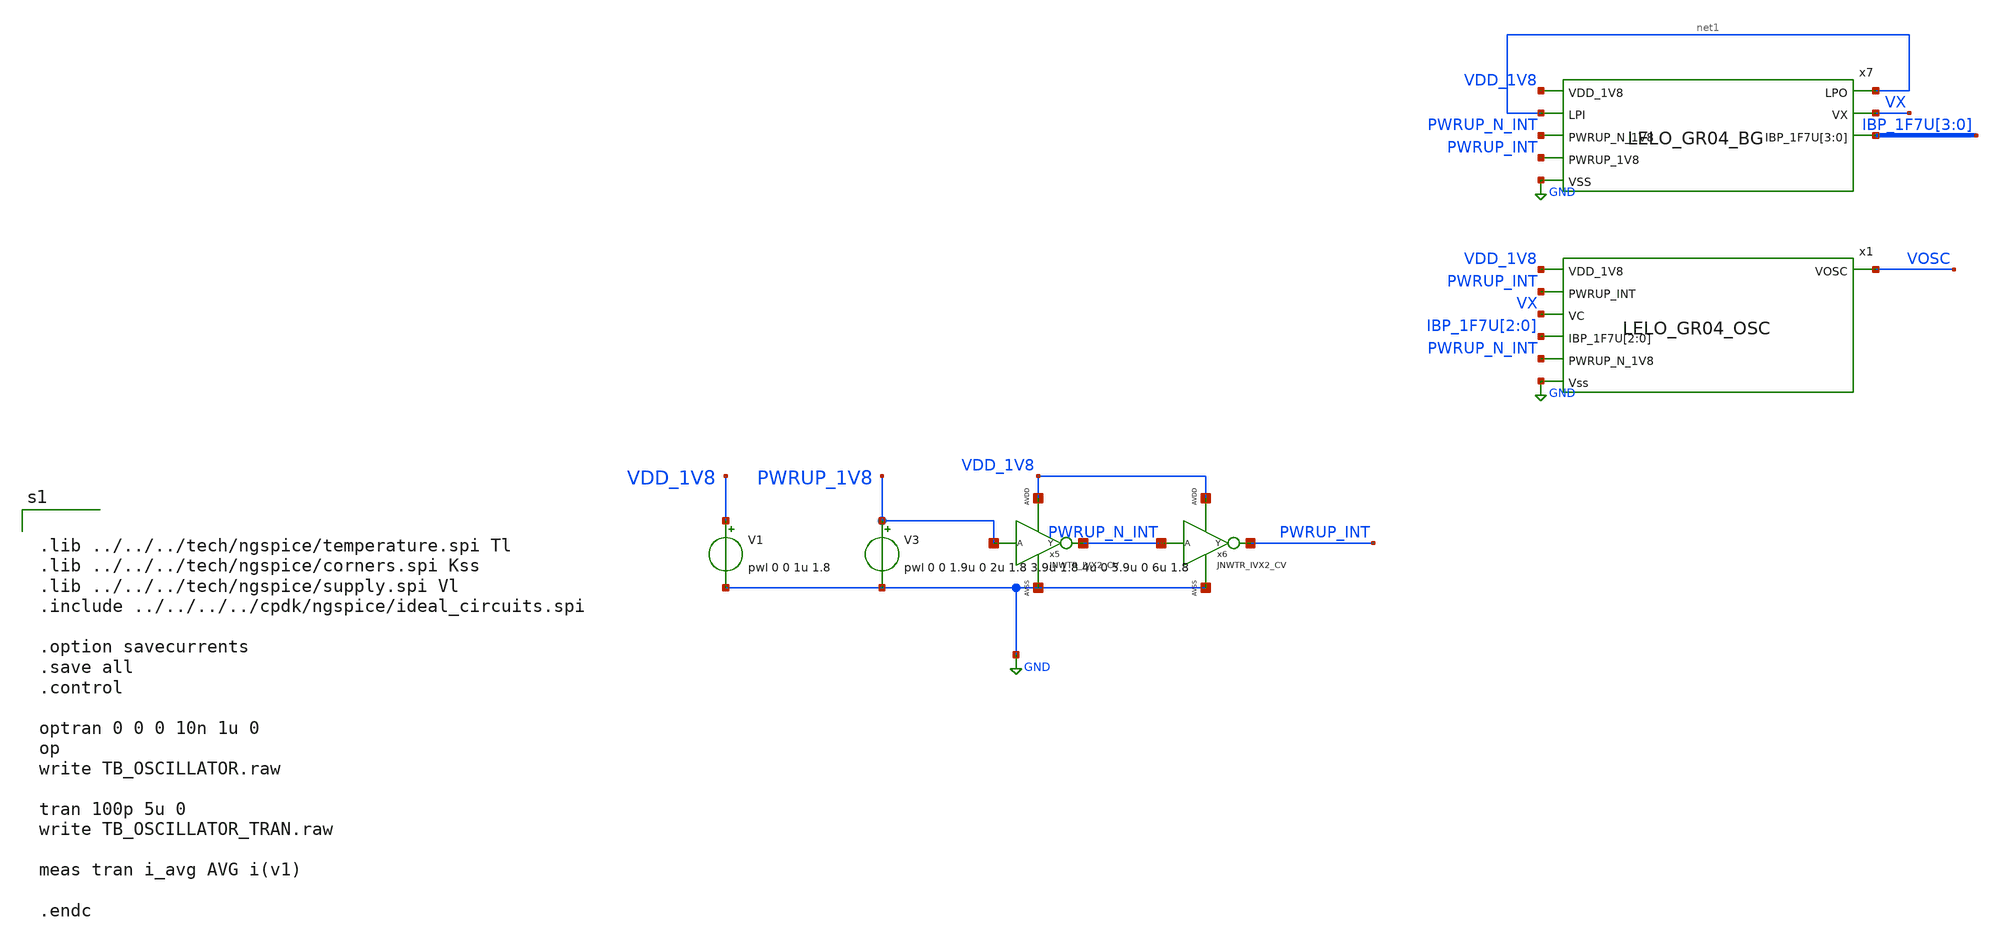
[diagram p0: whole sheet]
** sch_path: design/LELO_GR04_SKY130A/TB_OSCILLATOR.sch
**.subckt TB_OSCILLATOR
V1 VDD_1V8 GND pwl 0 0 1u 1.8
V3 PWRUP_1V8 GND pwl 0 0 1.9u 0 2u 1.8 3.9u 1.8 4u 0 5.9u 0 6u 1.8
x5 PWRUP_1V8 PWRUP_N_INT VDD_1V8 GND JNWTR_IVX2_CV xoffset=0 yoffset=0 angle=0 M=1
x6 PWRUP_N_INT PWRUP_INT VDD_1V8 GND JNWTR_IVX2_CV xoffset=0 yoffset=0 angle=0 M=1
x7 VDD_1V8 net1 net1 VX PWRUP_N_INT IBP_1F7U[3] IBP_1F7U[2] IBP_1F7U[1] IBP_1F7U[0] PWRUP_INT GND
+ LELO_GR04_BG
x1 VOSC VDD_1V8 PWRUP_INT VX IBP_1F7U[2] IBP_1F7U[1] IBP_1F7U[0] PWRUP_N_INT GND LELO_GR04_OSC
**** begin user architecture code


.lib ../../../tech/ngspice/temperature.spi Tl
.lib ../../../tech/ngspice/corners.spi Kss
.lib ../../../tech/ngspice/supply.spi Vl
.include ../../../../cpdk/ngspice/ideal_circuits.spi

.option savecurrents
.save all
.control

optran 0 0 0 10n 1u 0
op
write TB_OSCILLATOR.raw

tran 100p 5u 0
write TB_OSCILLATOR_TRAN.raw

meas tran i_avg AVG i(v1)

.endc


**** end user architecture code
**.ends
.GLOBAL GND
.end
